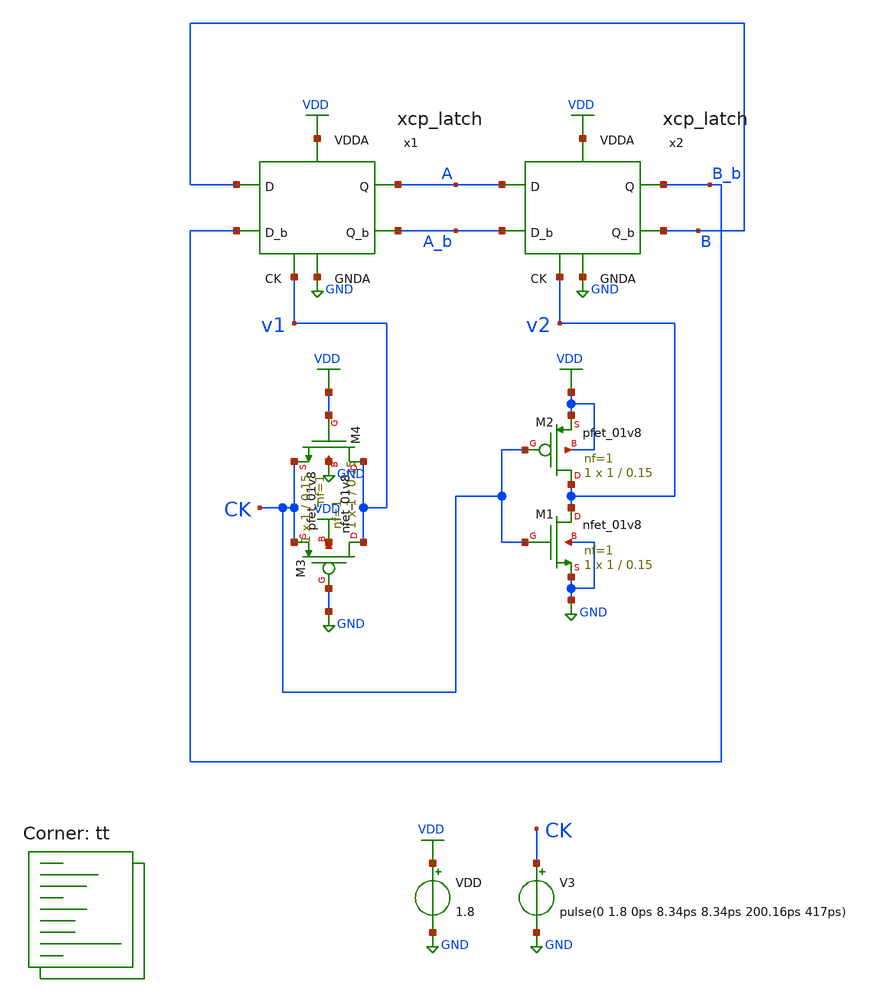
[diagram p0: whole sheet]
** sch_path: projects/pll/divider/xschem_ngspice/tb_xcp_latch.sch
**.subckt tb_xcp_latch
VDD VDD GND 1.8
V3 CK GND pulse(0 1.8 0ps 8.34ps 8.34ps 200.16ps 417ps)
x1 VDD A_b A B_b B v1 GND xcp_latch
x2 VDD B B_b A_b A v2 GND xcp_latch
XM1 v2 CK GND GND sky130_fd_pr__nfet_01v8 L=0.15 W=1 nf=1 ad='int((nf+1)/2) * W/nf * 0.29' as='int((nf+2)/2) * W/nf * 0.29'
+ pd='2*int((nf+1)/2) * (W/nf + 0.29)' ps='2*int((nf+2)/2) * (W/nf + 0.29)' nrd='0.29 / W' nrs='0.29 / W'
+ sa=0 sb=0 sd=0 mult=1 m=1
XM2 v2 CK VDD VDD sky130_fd_pr__pfet_01v8 L=0.15 W=1 nf=1 ad='int((nf+1)/2) * W/nf * 0.29' as='int((nf+2)/2) * W/nf * 0.29'
+ pd='2*int((nf+1)/2) * (W/nf + 0.29)' ps='2*int((nf+2)/2) * (W/nf + 0.29)' nrd='0.29 / W' nrs='0.29 / W'
+ sa=0 sb=0 sd=0 mult=1 m=1
XM3 v1 GND CK VDD sky130_fd_pr__pfet_01v8 L=0.15 W=1 nf=1 ad='int((nf+1)/2) * W/nf * 0.29' as='int((nf+2)/2) * W/nf * 0.29'
+ pd='2*int((nf+1)/2) * (W/nf + 0.29)' ps='2*int((nf+2)/2) * (W/nf + 0.29)' nrd='0.29 / W' nrs='0.29 / W'
+ sa=0 sb=0 sd=0 mult=1 m=1
XM4 v1 VDD CK GND sky130_fd_pr__nfet_01v8 L=0.15 W=1 nf=1 ad='int((nf+1)/2) * W/nf * 0.29' as='int((nf+2)/2) * W/nf * 0.29'
+ pd='2*int((nf+1)/2) * (W/nf + 0.29)' ps='2*int((nf+2)/2) * (W/nf + 0.29)' nrd='0.29 / W' nrs='0.29 / W'
+ sa=0 sb=0 sd=0 mult=1 m=1
**** begin user architecture code



.include /foss/pdks/sky130A/libs.ref/sky130_fd_sc_hd/spice/sky130_fd_sc_hd.spice

.option method=gear
.option wnflag=1
* .option savecurrents

.save @m.x1.xm1.msky130_fd_pr__nfet_01v8[gm] @m.x1.xm2.msky130_fd_pr__nfet_01v8[gm] @m.x1.xm3.msky130_fd_pr__pfet_01v8[gm] @m.x1.xm4.msky130_fd_pr__pfet_01v8[gm] @m.x1.xm5.msky130_fd_pr__nfet_01v8[gm] @m.x2.xm1.msky130_fd_pr__nfet_01v8[gm] @m.x2.xm2.msky130_fd_pr__nfet_01v8[gm] @m.x2.xm3.msky130_fd_pr__pfet_01v8[gm] @m.x2.xm4.msky130_fd_pr__pfet_01v8[gm] @m.x2.xm5.msky130_fd_pr__nfet_01v8[gm] @v.x1.vmeas @v.x1.vmeas1 @v.x1.vmeas2 @v.x5.vmeas @v.x5.vmeas1 @v.x5.vmeas2


*.ic v(b)=0

.control

  save v(a) v(a_b) v(b) v(b_b) v(ck) v(ck_b) v(v1) v(v2) v(gnd) v(vdd)
  * save all
  *tran 0.1n 1u
  tran 0.2p 10n
  *ac dec 20 1 1T
  remzerovec
  write tb_xcp_latch.raw
  set appendwrite

.endc



.lib $::SKYWATER_MODELS/sky130.lib.spice tt
**** end user architecture code
**.ends

* expanding   symbol:  /foss/designs/my_design/projects/pll/divider/xschem_ngspice/xcp_latch.sym #
*+ of pins=7
** sym_path: projects/pll/divider/xschem_ngspice/xcp_latch.sym
** sch_path: projects/pll/divider/xschem_ngspice/xcp_latch.sch
.subckt xcp_latch VDDA Q_b Q D_b D CK GNDA
*.ipin D
*.opin Q
*.ipin D_b
*.ipin CK
*.opin Q_b
*.ipin VDDA
*.ipin GNDA
XM5 net1 CK GNDA GNDA sky130_fd_pr__nfet_01v8 L=0.15 W=2 nf=2 ad='int((nf+1)/2) * W/nf * 0.29' as='int((nf+2)/2) * W/nf * 0.29'
+ pd='2*int((nf+1)/2) * (W/nf + 0.29)' ps='2*int((nf+2)/2) * (W/nf + 0.29)' nrd='0.29 / W' nrs='0.29 / W'
+ sa=0 sb=0 sd=0 mult=1 m=1
XM1 net3 D V_common GNDA sky130_fd_pr__nfet_01v8 L=0.15 W=1 nf=1 ad='int((nf+1)/2) * W/nf * 0.29' as='int((nf+2)/2) * W/nf * 0.29'
+ pd='2*int((nf+1)/2) * (W/nf + 0.29)' ps='2*int((nf+2)/2) * (W/nf + 0.29)' nrd='0.29 / W' nrs='0.29 / W'
+ sa=0 sb=0 sd=0 mult=1 m=1
XM2 net2 D_b V_common GNDA sky130_fd_pr__nfet_01v8 L=0.15 W=1 nf=1 ad='int((nf+1)/2) * W/nf * 0.29' as='int((nf+2)/2) * W/nf * 0.29'
+ pd='2*int((nf+1)/2) * (W/nf + 0.29)' ps='2*int((nf+2)/2) * (W/nf + 0.29)' nrd='0.29 / W' nrs='0.29 / W'
+ sa=0 sb=0 sd=0 mult=1 m=1
Vmeas V_common net1 0
.save i(vmeas)
Vmeas1 Q_b net3 0
.save i(vmeas1)
Vmeas2 Q net2 0
.save i(vmeas2)
XM3 Q_b Q VDDA VDDA sky130_fd_pr__pfet_01v8 L=0.15 W=1 nf=1 ad='int((nf+1)/2) * W/nf * 0.29' as='int((nf+2)/2) * W/nf * 0.29'
+ pd='2*int((nf+1)/2) * (W/nf + 0.29)' ps='2*int((nf+2)/2) * (W/nf + 0.29)' nrd='0.29 / W' nrs='0.29 / W'
+ sa=0 sb=0 sd=0 mult=1 m=1
XM4 Q Q_b VDDA VDDA sky130_fd_pr__pfet_01v8 L=0.15 W=1 nf=1 ad='int((nf+1)/2) * W/nf * 0.29' as='int((nf+2)/2) * W/nf * 0.29'
+ pd='2*int((nf+1)/2) * (W/nf + 0.29)' ps='2*int((nf+2)/2) * (W/nf + 0.29)' nrd='0.29 / W' nrs='0.29 / W'
+ sa=0 sb=0 sd=0 mult=1 m=1
.ends

.GLOBAL GND
.GLOBAL VDD
.end
